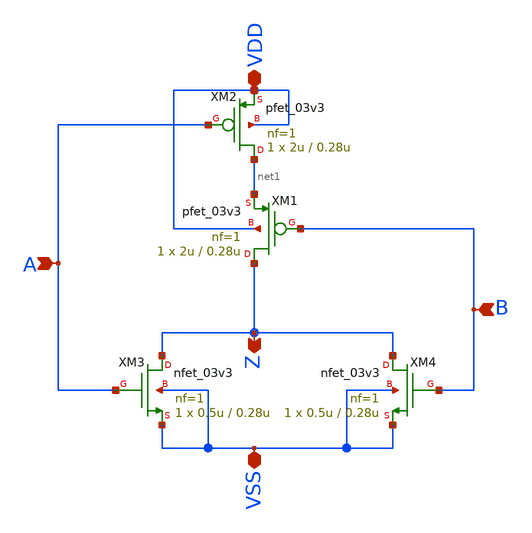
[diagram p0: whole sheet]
** sch_path: sar_logic/sar_designs/nor2/nor2.sch
**.subckt nor2 VSS VDD A B Z
*.iopin VSS
*.iopin VDD
*.ipin A
*.ipin B
*.opin Z
XM1 Z B net1 VDD pfet_03v3 L=0.28u W=2u nf=1 ad='int((nf+1)/2) * W/nf * 0.18u' as='int((nf+2)/2) * W/nf * 0.18u'
+ pd='2*int((nf+1)/2) * (W/nf + 0.18u)' ps='2*int((nf+2)/2) * (W/nf + 0.18u)' nrd='0.18u / W' nrs='0.18u / W'
+ sa=0 sb=0 sd=0 m=1
XM2 net1 A VDD VDD pfet_03v3 L=0.28u W=2u nf=1 ad='int((nf+1)/2) * W/nf * 0.18u' as='int((nf+2)/2) * W/nf * 0.18u'
+ pd='2*int((nf+1)/2) * (W/nf + 0.18u)' ps='2*int((nf+2)/2) * (W/nf + 0.18u)' nrd='0.18u / W' nrs='0.18u / W'
+ sa=0 sb=0 sd=0 m=1
XM3 Z A VSS VSS nfet_03v3 L=0.28u W=0.5u nf=1 ad='int((nf+1)/2) * W/nf * 0.18u' as='int((nf+2)/2) * W/nf * 0.18u'
+ pd='2*int((nf+1)/2) * (W/nf + 0.18u)' ps='2*int((nf+2)/2) * (W/nf + 0.18u)' nrd='0.18u / W' nrs='0.18u / W'
+ sa=0 sb=0 sd=0 m=1
XM4 Z B VSS VSS nfet_03v3 L=0.28u W=0.5u nf=1 ad='int((nf+1)/2) * W/nf * 0.18u' as='int((nf+2)/2) * W/nf * 0.18u'
+ pd='2*int((nf+1)/2) * (W/nf + 0.18u)' ps='2*int((nf+2)/2) * (W/nf + 0.18u)' nrd='0.18u / W' nrs='0.18u / W'
+ sa=0 sb=0 sd=0 m=1
**.ends
.end
